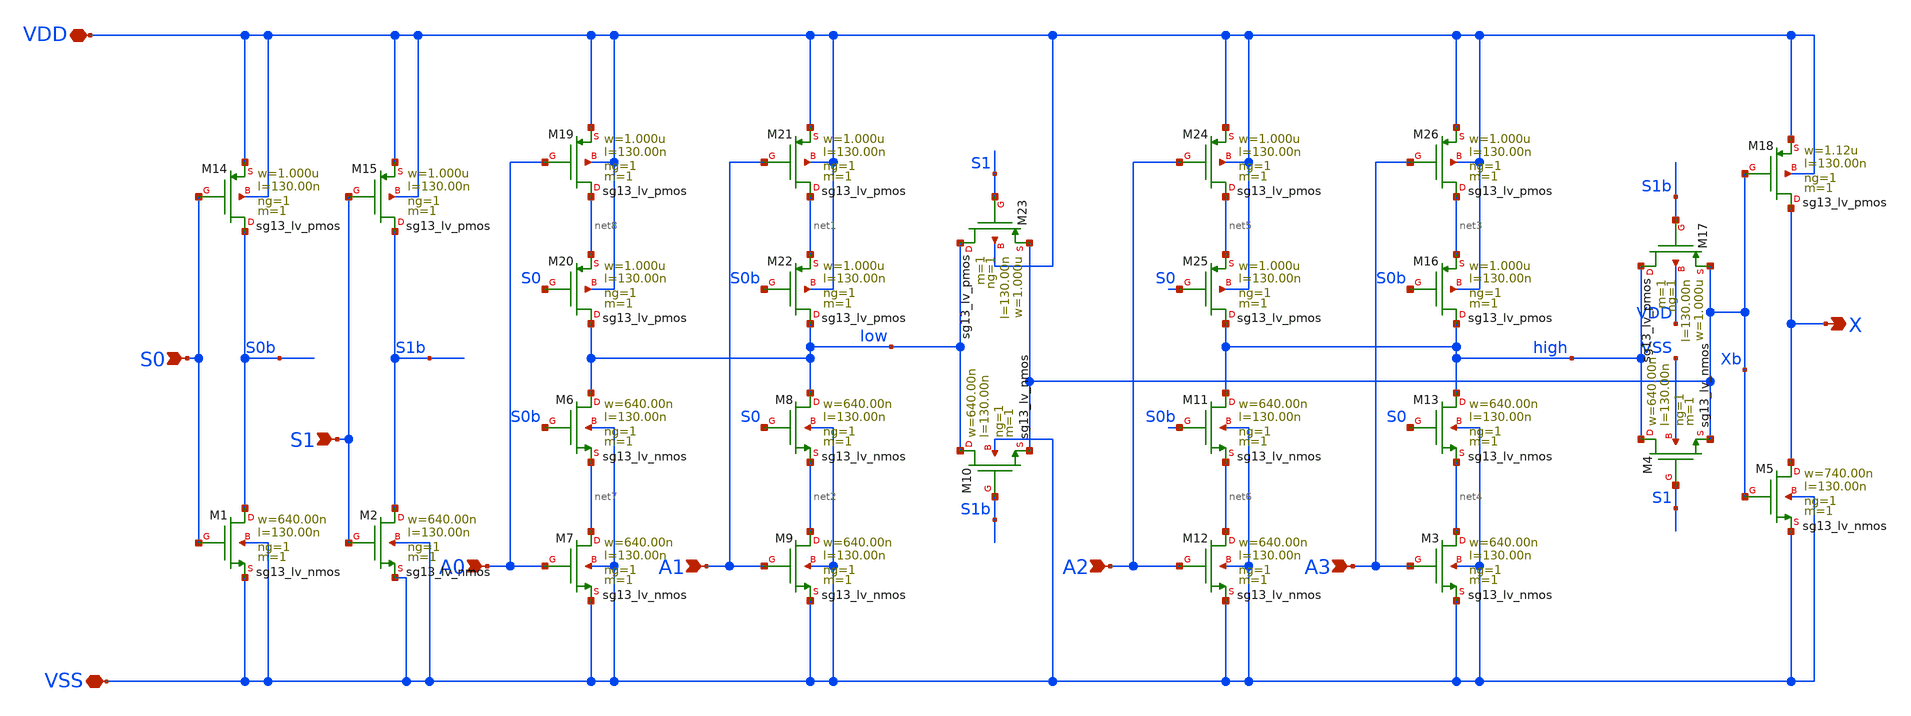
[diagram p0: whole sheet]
** sch_path: ihp-sg13g2/libs.tech/xschem/sg13g2_stdcells/sg13g2_mux4_1.sch
* Copyright 2023 IHP PDK Authors
* Licensed under the Apache License, Version 2.0 (the "License");
* you may not use this file except in compliance with the License.
* You may obtain a copy of the License at
* https://www.apache.org/licenses/LICENSE-2.0
* Unless required by applicable law or agreed to in writing, software
* distributed under the License is distributed on an "AS IS" BASIS,
* WITHOUT WARRANTIES OR CONDITIONS OF ANY KIND, either express or implied.
* See the License for the specific language governing permissions and
* limitations under the License.
**.subckt sg13g2_mux4_1 S0 S1 VSS A0 A1 A2 A3 X VDD
*.ipin S0
*.ipin S1
*.iopin VSS
*.ipin A0
*.ipin A1
*.ipin A2
*.ipin A3
*.opin X
*.iopin VDD
XM1 S0b S0 VSS VSS sg13_lv_nmos w=640.00n l=130.00n ng=1 m=1 mm_ok=1
XM2 S1b S1 VSS VSS sg13_lv_nmos w=640.00n l=130.00n ng=1 m=1 mm_ok=1
XM3 net4 A3 VSS VSS sg13_lv_nmos w=640.00n l=130.00n ng=1 m=1 mm_ok=1
XM4 high S1 Xb VSS sg13_lv_nmos w=640.00n l=130.00n ng=1 m=1 mm_ok=1
XM5 X Xb VSS VSS sg13_lv_nmos w=740.00n l=130.00n ng=1 m=1 mm_ok=1
XM6 low S0b net7 VSS sg13_lv_nmos w=640.00n l=130.00n ng=1 m=1 mm_ok=1
XM7 net7 A0 VSS VSS sg13_lv_nmos w=640.00n l=130.00n ng=1 m=1 mm_ok=1
XM8 low S0 net2 VSS sg13_lv_nmos w=640.00n l=130.00n ng=1 m=1 mm_ok=1
XM9 net2 A1 VSS VSS sg13_lv_nmos w=640.00n l=130.00n ng=1 m=1 mm_ok=1
XM10 low S1b Xb VSS sg13_lv_nmos w=640.00n l=130.00n ng=1 m=1 mm_ok=1
XM11 high S0b net6 VSS sg13_lv_nmos w=640.00n l=130.00n ng=1 m=1 mm_ok=1
XM12 net6 A2 VSS VSS sg13_lv_nmos w=640.00n l=130.00n ng=1 m=1 mm_ok=1
XM13 high S0 net4 VSS sg13_lv_nmos w=640.00n l=130.00n ng=1 m=1 mm_ok=1
XM14 S0b S0 VDD VDD sg13_lv_pmos w=1.000u l=130.00n ng=1 m=1 mm_ok=1
XM15 S1b S1 VDD VDD sg13_lv_pmos w=1.000u l=130.00n ng=1 m=1 mm_ok=1
XM16 high S0b net3 VDD sg13_lv_pmos w=1.000u l=130.00n ng=1 m=1 mm_ok=1
XM17 high S1b Xb VDD sg13_lv_pmos w=1.000u l=130.00n ng=1 m=1 mm_ok=1
XM18 X Xb VDD VDD sg13_lv_pmos w=1.12u l=130.00n ng=1 m=1 mm_ok=1
XM19 net8 A0 VDD VDD sg13_lv_pmos w=1.000u l=130.00n ng=1 m=1 mm_ok=1
XM20 low S0 net8 VDD sg13_lv_pmos w=1.000u l=130.00n ng=1 m=1 mm_ok=1
XM21 net1 A1 VDD VDD sg13_lv_pmos w=1.000u l=130.00n ng=1 m=1 mm_ok=1
XM22 low S0b net1 VDD sg13_lv_pmos w=1.000u l=130.00n ng=1 m=1 mm_ok=1
XM23 low S1 Xb VDD sg13_lv_pmos w=1.000u l=130.00n ng=1 m=1 mm_ok=1
XM24 net5 A2 VDD VDD sg13_lv_pmos w=1.000u l=130.00n ng=1 m=1 mm_ok=1
XM25 high S0 net5 VDD sg13_lv_pmos w=1.000u l=130.00n ng=1 m=1 mm_ok=1
XM26 net3 A3 VDD VDD sg13_lv_pmos w=1.000u l=130.00n ng=1 m=1 mm_ok=1
**.ends
.end
